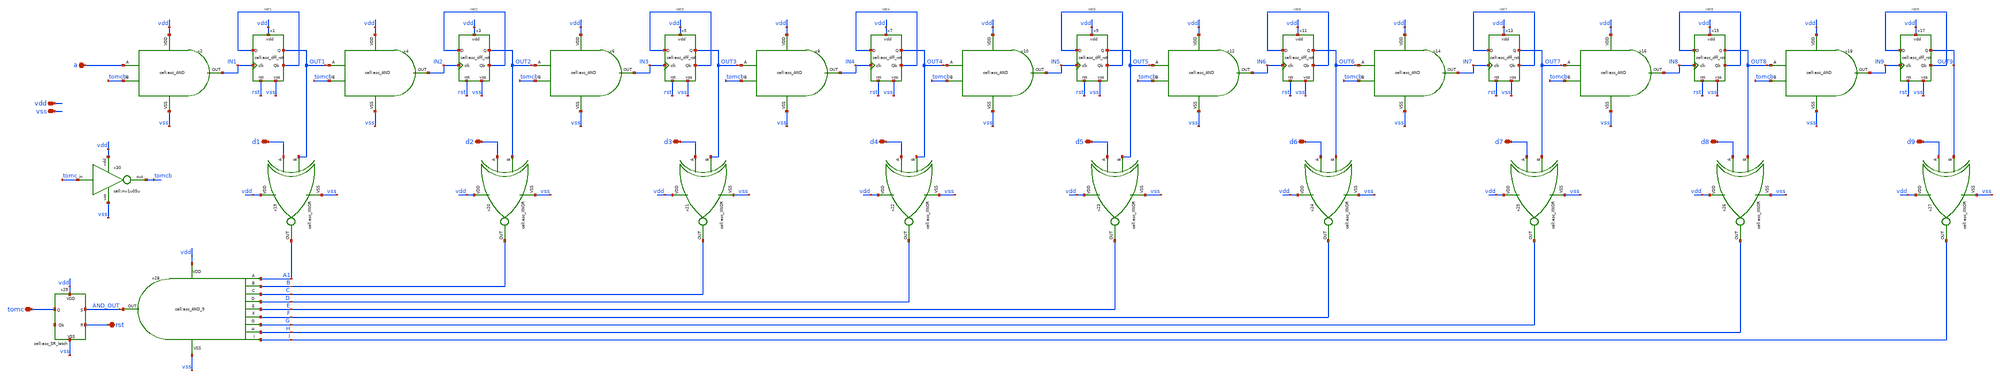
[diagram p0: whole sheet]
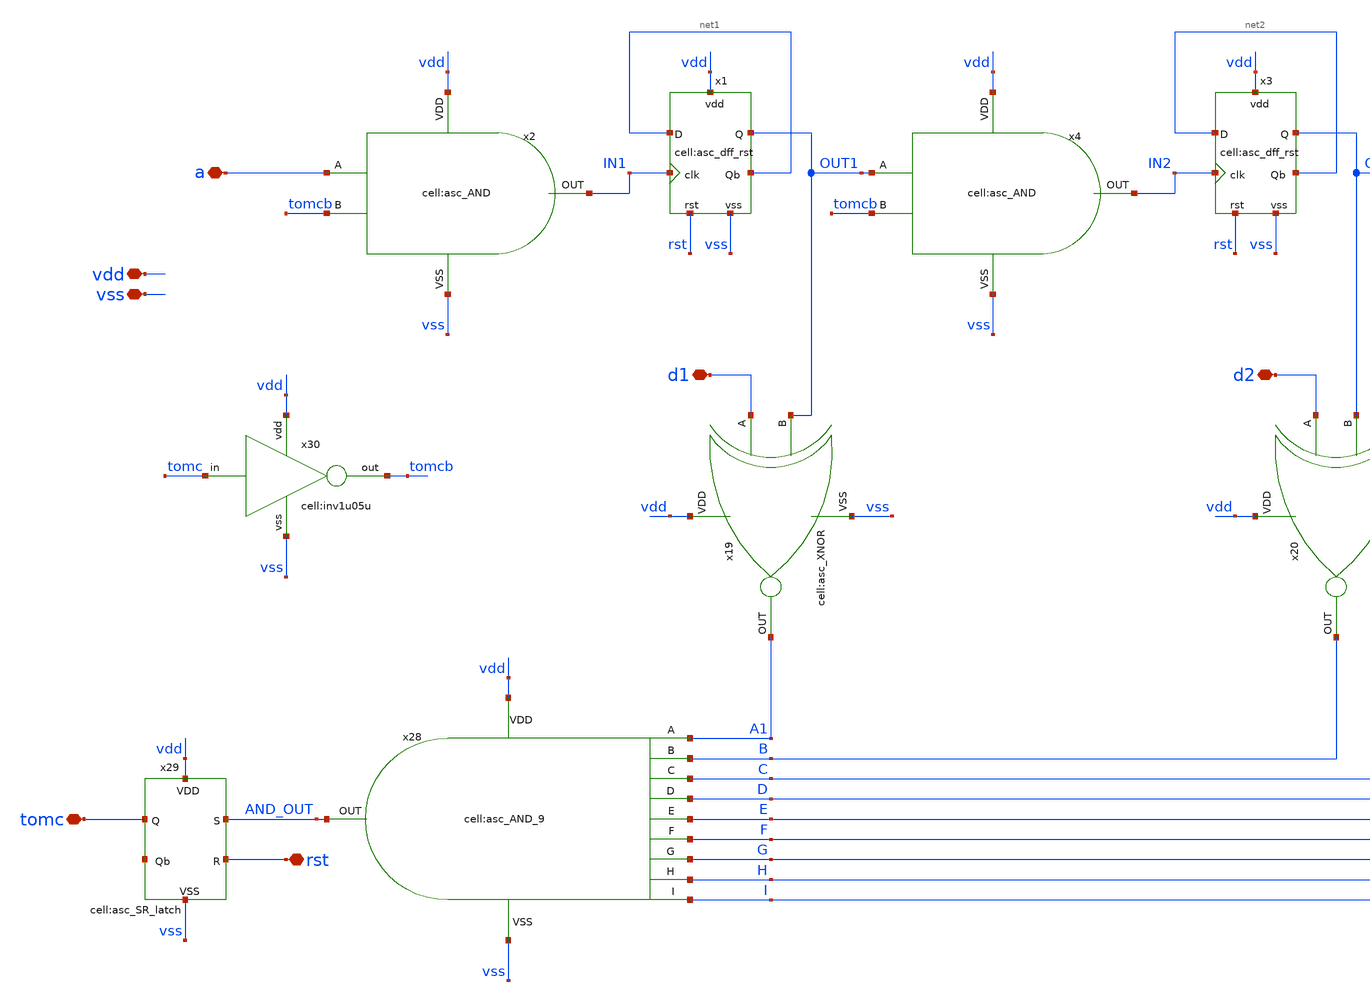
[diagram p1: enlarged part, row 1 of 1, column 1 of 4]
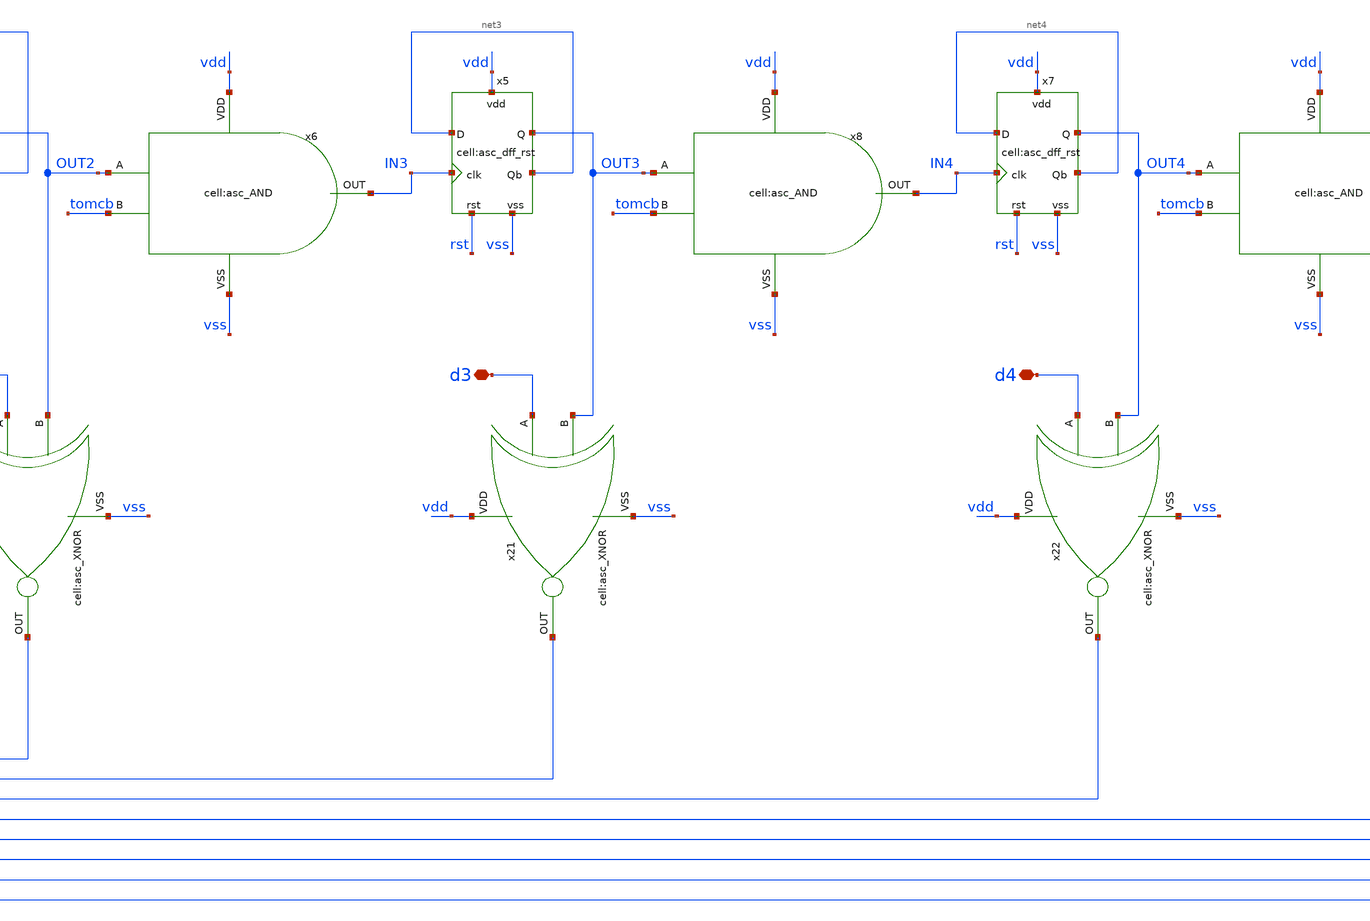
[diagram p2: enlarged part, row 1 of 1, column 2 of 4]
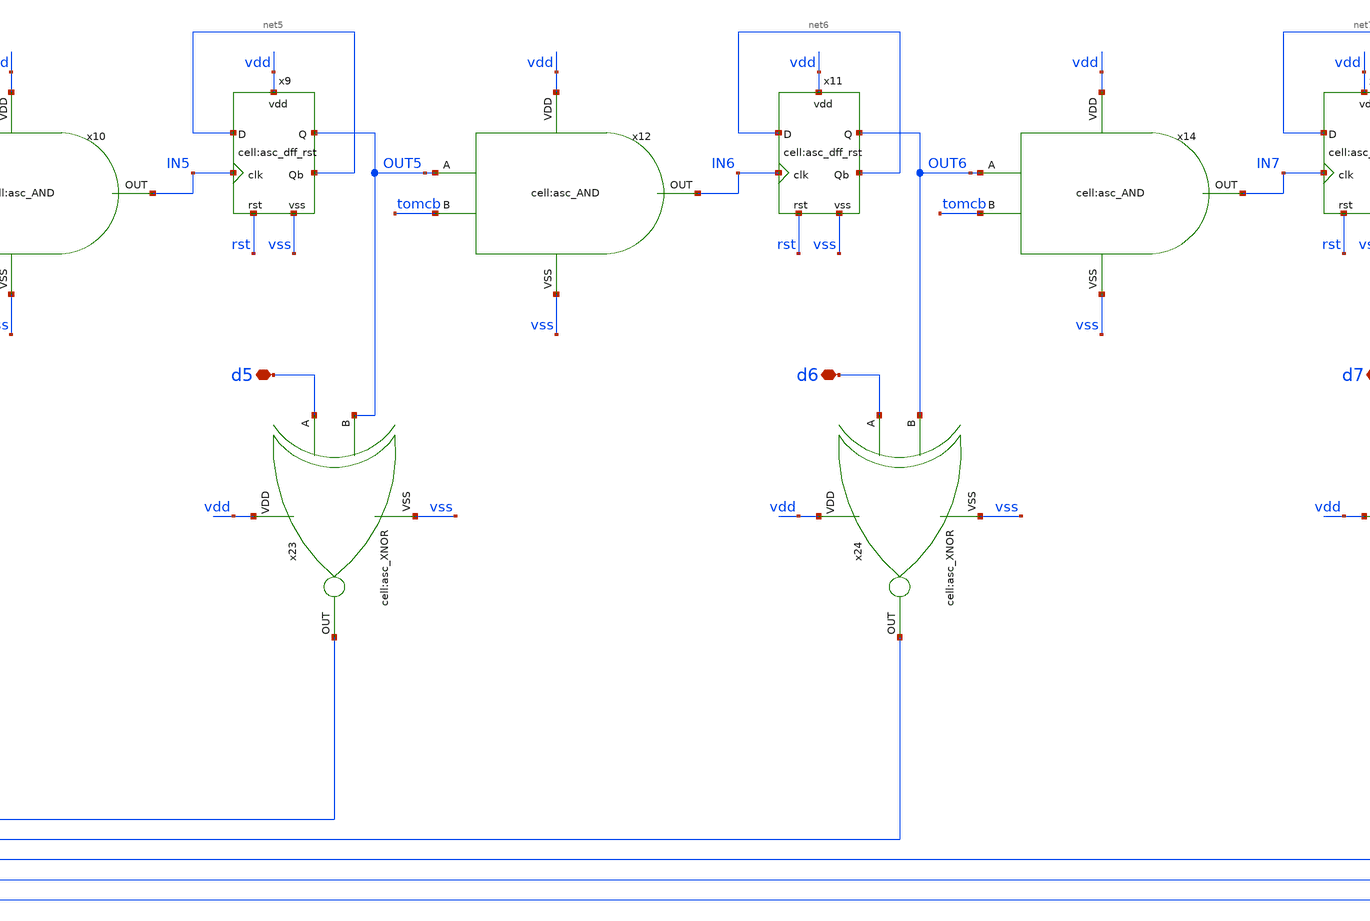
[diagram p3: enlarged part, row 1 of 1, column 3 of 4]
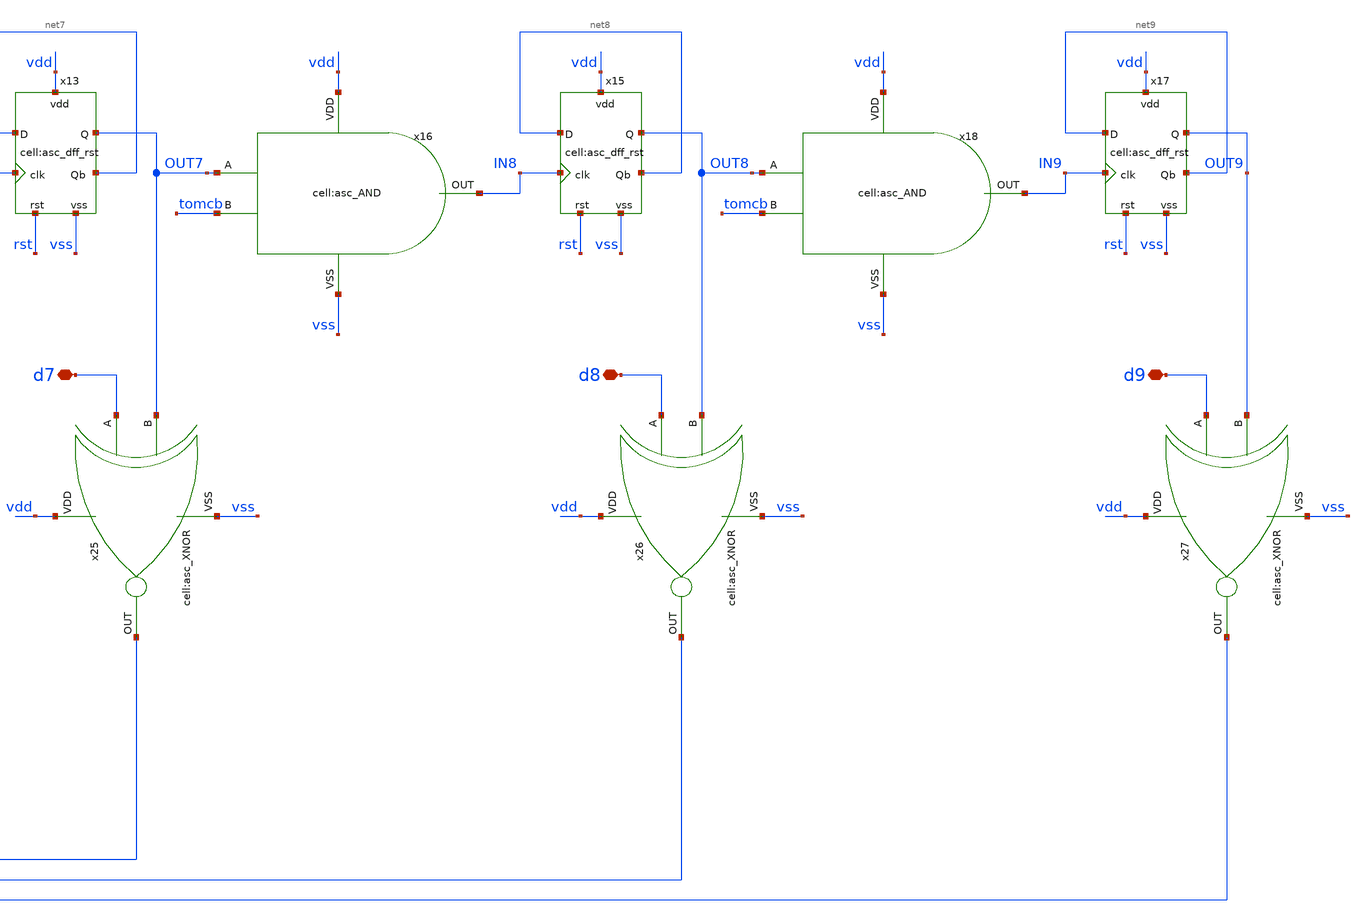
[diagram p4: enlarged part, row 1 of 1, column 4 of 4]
** sch_path: designs/libs/xp_core_analog/asc_swallow_counter_rst/asc_swallow_counter_rst.sch
**.subckt asc_swallow_counter_rst a vdd vss tomc d1 d2 d3 d4 d5 d6 d7 d8 d9 rst
*.iopin a
*.iopin vdd
*.iopin vss
*.iopin tomc
*.iopin d1
*.iopin d2
*.iopin d3
*.iopin d4
*.iopin d5
*.iopin d6
*.iopin d7
*.iopin d8
*.iopin d9
*.iopin rst
x2 vdd IN1 a tomcb vss asc_AND
x4 vdd IN2 OUT1 tomcb vss asc_AND
x6 vdd IN3 OUT2 tomcb vss asc_AND
x8 vdd IN4 OUT3 tomcb vss asc_AND
x10 vdd IN5 OUT4 tomcb vss asc_AND
x12 vdd IN6 OUT5 tomcb vss asc_AND
x14 vdd IN7 OUT6 tomcb vss asc_AND
x16 vdd IN8 OUT7 tomcb vss asc_AND
x18 vdd IN9 OUT8 tomcb vss asc_AND
x19 vdd vss A1 d1 OUT1 asc_XNOR
x20 vdd vss B d2 OUT2 asc_XNOR
x21 vdd vss C d3 OUT3 asc_XNOR
x22 vdd vss D d4 OUT4 asc_XNOR
x23 vdd vss E d5 OUT5 asc_XNOR
x24 vdd vss F d6 OUT6 asc_XNOR
x25 vdd vss G d7 OUT7 asc_XNOR
x26 vdd vss H d8 OUT8 asc_XNOR
x27 vdd vss I d9 OUT9 asc_XNOR
x28 vdd vss AND_OUT A1 B C D E F G H I asc_AND_9
x29 rst AND_OUT net10 vdd vss tomc asc_SR_latch
x30 tomc vdd tomcb vss inv1u05u
x1 IN1 net1 net1 vdd vss OUT1 rst asc_dff_rst
x3 IN2 net2 net2 vdd vss OUT2 rst asc_dff_rst
x5 IN3 net3 net3 vdd vss OUT3 rst asc_dff_rst
x7 IN4 net4 net4 vdd vss OUT4 rst asc_dff_rst
x9 IN5 net5 net5 vdd vss OUT5 rst asc_dff_rst
x11 IN6 net6 net6 vdd vss OUT6 rst asc_dff_rst
x13 IN7 net7 net7 vdd vss OUT7 rst asc_dff_rst
x15 IN8 net8 net8 vdd vss OUT8 rst asc_dff_rst
x17 IN9 net9 net9 vdd vss OUT9 rst asc_dff_rst
**.ends
.end
